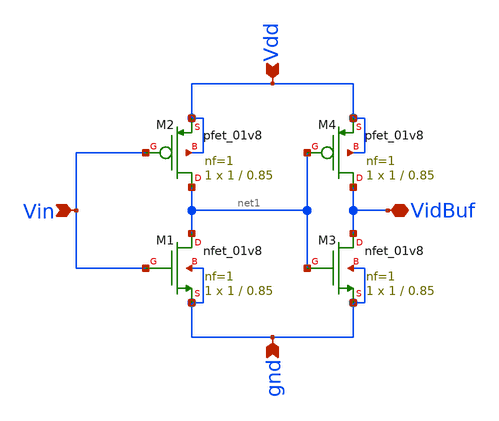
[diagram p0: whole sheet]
** sch_path: xschem/analog_desing/Buffer/Buffer.sch
**.subckt Buffer VidBuf Vin Vdd gnd
*.iopin VidBuf
*.ipin Vin
*.ipin Vdd
*.ipin gnd
XM1 net1 Vin gnd gnd sky130_fd_pr__nfet_01v8 L=0.85 W=1 nf=1 ad='int((nf+1)/2) * W/nf * 0.29' as='int((nf+2)/2) * W/nf * 0.29'
+ pd='2*int((nf+1)/2) * (W/nf + 0.29)' ps='2*int((nf+2)/2) * (W/nf + 0.29)' nrd='0.29 / W' nrs='0.29 / W'
+ sa=0 sb=0 sd=0 mult=1 m=1
XM2 net1 Vin Vdd Vdd sky130_fd_pr__pfet_01v8 L=0.85 W=1 nf=1 ad='int((nf+1)/2) * W/nf * 0.29' as='int((nf+2)/2) * W/nf * 0.29'
+ pd='2*int((nf+1)/2) * (W/nf + 0.29)' ps='2*int((nf+2)/2) * (W/nf + 0.29)' nrd='0.29 / W' nrs='0.29 / W'
+ sa=0 sb=0 sd=0 mult=1 m=1
XM3 VidBuf net1 gnd gnd sky130_fd_pr__nfet_01v8 L=0.85 W=1 nf=1 ad='int((nf+1)/2) * W/nf * 0.29' as='int((nf+2)/2) * W/nf * 0.29'
+ pd='2*int((nf+1)/2) * (W/nf + 0.29)' ps='2*int((nf+2)/2) * (W/nf + 0.29)' nrd='0.29 / W' nrs='0.29 / W'
+ sa=0 sb=0 sd=0 mult=1 m=1
XM4 VidBuf net1 Vdd Vdd sky130_fd_pr__pfet_01v8 L=0.85 W=1 nf=1 ad='int((nf+1)/2) * W/nf * 0.29' as='int((nf+2)/2) * W/nf * 0.29'
+ pd='2*int((nf+1)/2) * (W/nf + 0.29)' ps='2*int((nf+2)/2) * (W/nf + 0.29)' nrd='0.29 / W' nrs='0.29 / W'
+ sa=0 sb=0 sd=0 mult=1 m=1
**.ends
.end
